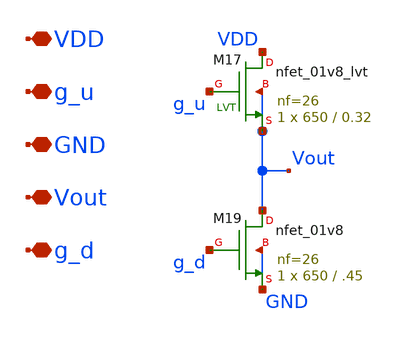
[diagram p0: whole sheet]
** sch_path: xschem/sf_half.sch
**.subckt sf_half VDD g_u GND Vout g_d
*.iopin VDD
*.iopin g_u
*.iopin GND
*.iopin Vout
*.iopin g_d
XM17 VDD g_u Vout Vout sky130_fd_pr__nfet_01v8_lvt L=0.32 W=650 nf=26 ad='int((nf+1)/2) * W/nf * 0.29'
+ as='int((nf+2)/2) * W/nf * 0.29' pd='2*int((nf+1)/2) * (W/nf + 0.29)' ps='2*int((nf+2)/2) * (W/nf + 0.29)'
+ nrd='0.29 / W' nrs='0.29 / W' sa=0 sb=0 sd=0 mult=1 m=1
XM19 Vout g_d GND GND sky130_fd_pr__nfet_01v8 L=.45 W=650 nf=26 ad='int((nf+1)/2) * W/nf * 0.29' as='int((nf+2)/2) * W/nf * 0.29'
+ pd='2*int((nf+1)/2) * (W/nf + 0.29)' ps='2*int((nf+2)/2) * (W/nf + 0.29)' nrd='0.29 / W' nrs='0.29 / W'
+ sa=0 sb=0 sd=0 mult=1 m=1
**.ends
.end
